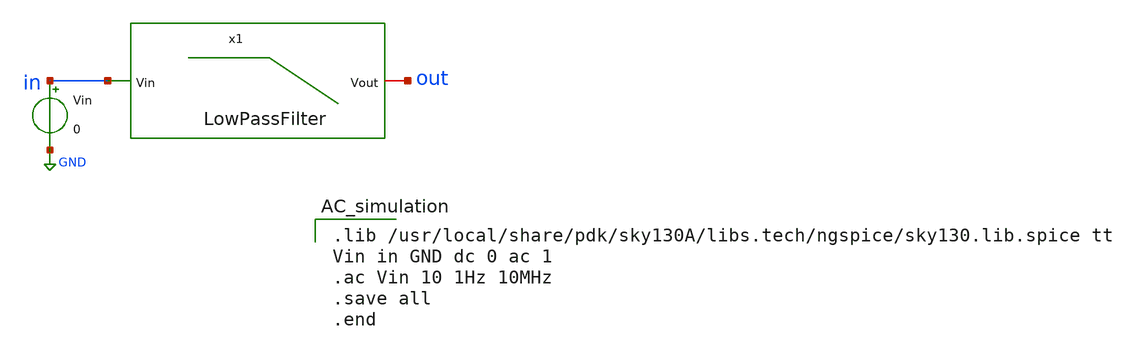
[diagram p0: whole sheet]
** sch_path: xschem/analog_desing/Filtro/LowPassFilter_tb.sch
**.subckt LowPassFilter_tb
x1 out in LowPassFilter
Vin in GND 0
**** begin user architecture code

.lib /usr/local/share/pdk/sky130A/libs.tech/ngspice/sky130.lib.spice tt
Vin in GND dc 0 ac 1
.ac Vin 10 1Hz 10MHz
.save all
.end

**** end user architecture code
**.ends

* expanding   symbol:  /home/celina/Tesis/xschem/analog_desing/Filtro/LowPassFilter.sym # of pins=2
** sym_path: xschem/analog_desing/Filtro/LowPassFilter.sym
** sch_path: xschem/analog_desing/Filtro/LowPassFilter.sch
.subckt LowPassFilter Vout Vin
*.ipin Vin
*.iopin Vout
XC1 Vout GND sky130_fd_pr__cap_mim_m3_1 W=1 L=1 MF=1 m=1
XR1 Vout Vin sky130_fd_pr__res_generic_po W=0.0482 L=10 m=1
.ends

.GLOBAL GND
.end
